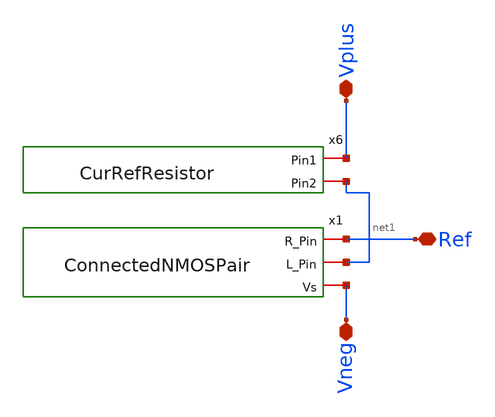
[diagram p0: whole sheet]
** sch_path: xschem/PrimalStructures/Level2/CurrentRef.sch
**.subckt CurrentRef Vplus Ref Vneg
*.iopin Vplus
*.iopin Ref
*.iopin Vneg
x6 Vplus net1 CurRefResistor
x1 Ref net1 Vneg ConnectedNMOSPair
**** begin user architecture code

** opencircuitdesign pdks install
.lib $::SKYWATER_MODELS/sky130.lib.spice tt


**** end user architecture code
**.ends
.end
